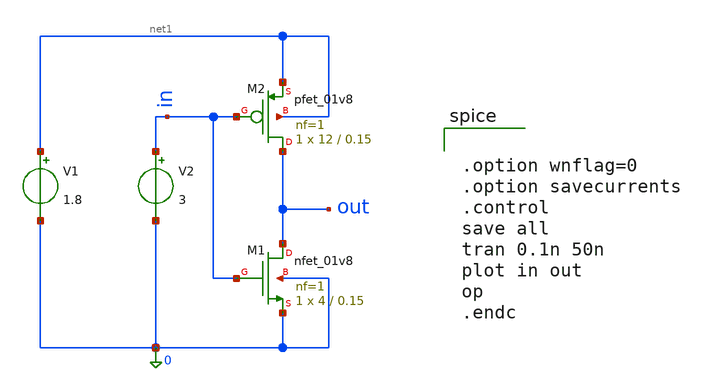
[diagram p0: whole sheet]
** sch_path: inverter-dc-transient/tugas1.sch
**.subckt tugas1
XM1 out in 0 0 sky130_fd_pr__nfet_01v8 L=0.15 W=4 nf=1 ad='int((1 + 1)/2) * 4 / 1 * 0.29' as='int((1 + 2)/2) * 4 / 1 * 0.29'
+ pd='2*int((1 + 1)/2) * (4 / 1 + 0.29)' ps='2*int((1 + 2)/2) * (4 / 1 + 0.29)' nrd='0.29 / 4 ' nrs='0.29 / 4 '
+ sa=0 sb=0 sd=0 mult=1 m=1
XM2 out in net1 net1 sky130_fd_pr__pfet_01v8 L=0.15 W=12 nf=1 ad='int((1 + 1)/2) * 12 / 1 * 0.29' as='int((1 + 2)/2) * 12 / 1 * 0.29'
+ pd='2*int((1 + 1)/2) * (12 / 1 + 0.29)' ps='2*int((1 + 2)/2) * (12 / 1 + 0.29)' nrd='0.29 / 12 ' nrs='0.29 / 12 '
+ sa=0 sb=0 sd=0 mult=1 m=1
V1 net1 0 1.8
V2 in 0 3
**** begin user architecture code

** opencircuitdesign pdks install
.lib $::SKYWATER_MODELS/sky130.lib.spice tt
.param mc_mm_switch = 0
.param mc_pr_switch = 1



.option wnflag=0
.option savecurrents
.control
save all
tran 0.1n 50n
plot in out
op
.endc


**** end user architecture code
**.ends
.end
